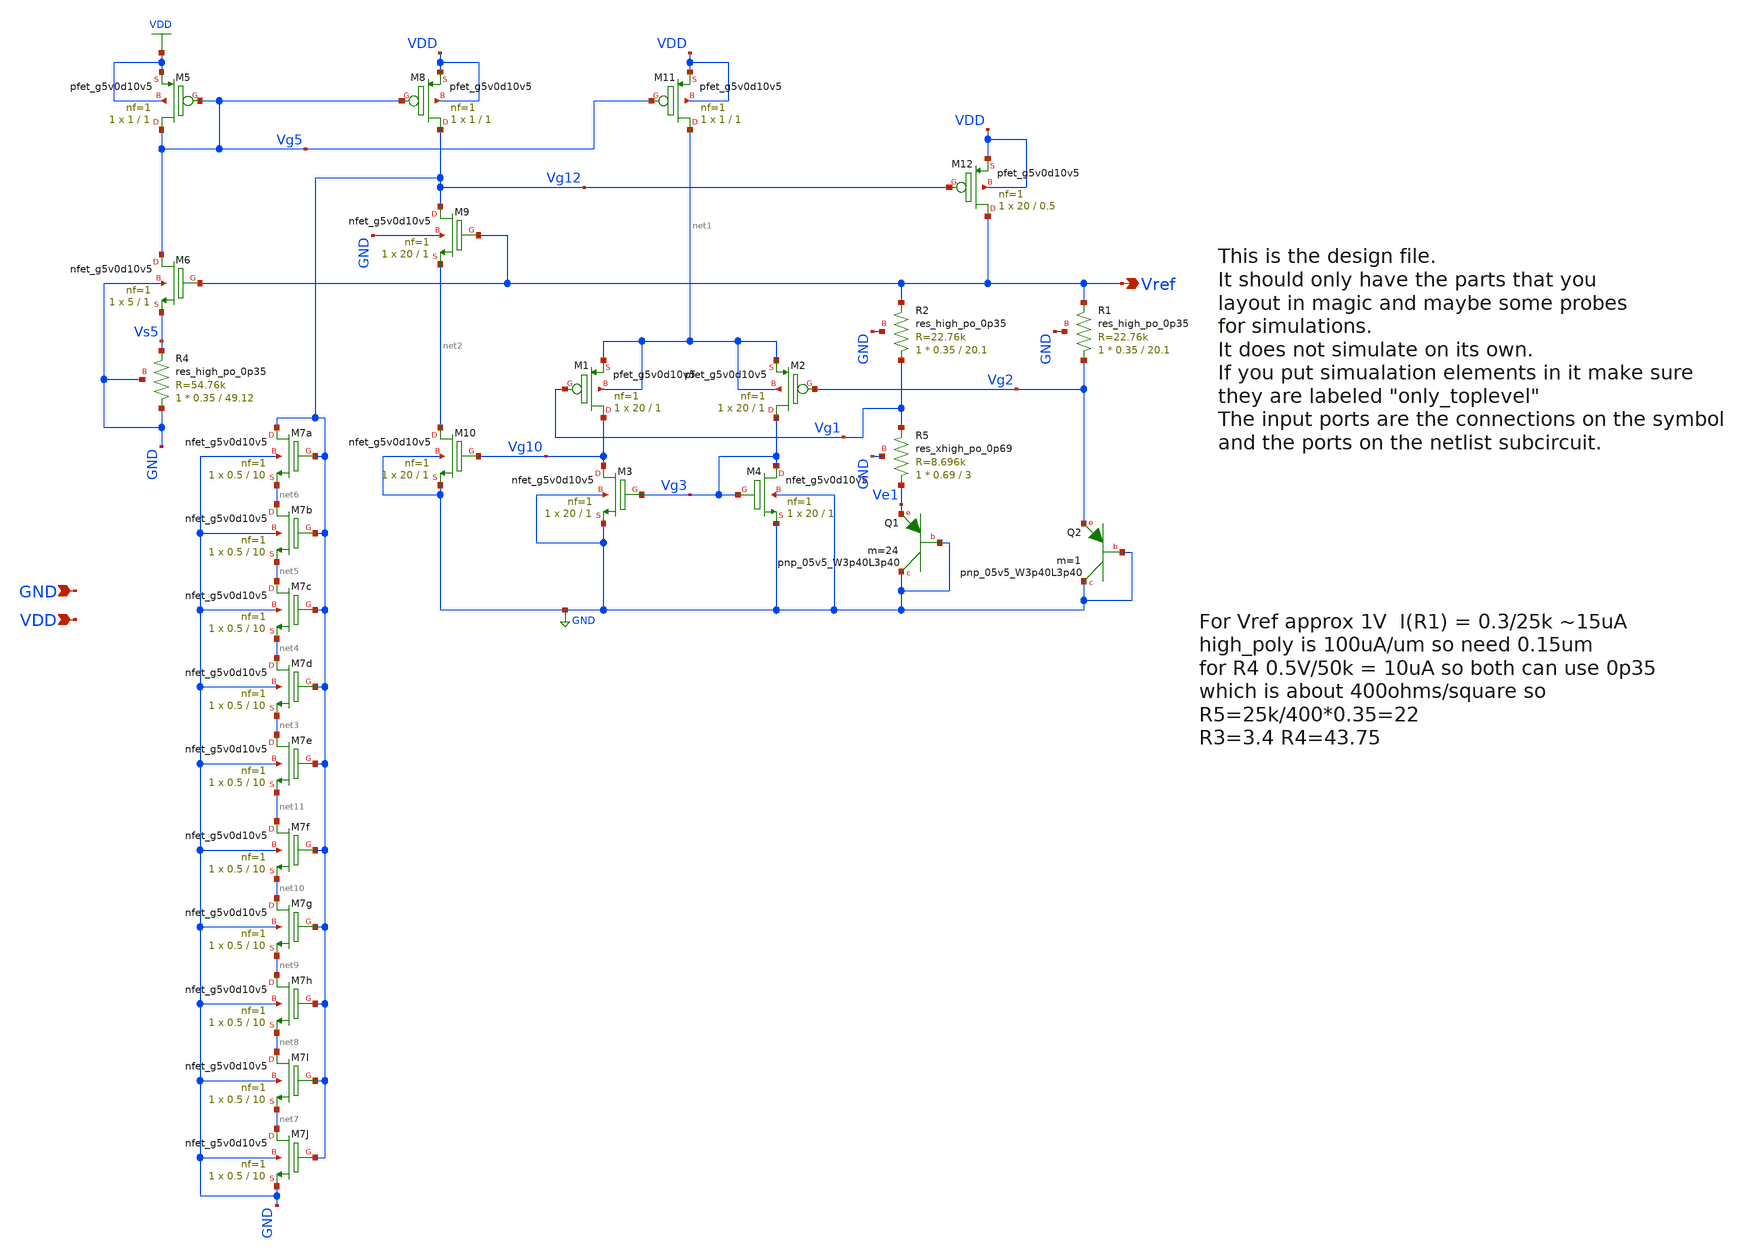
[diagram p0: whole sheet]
** sch_path: xschem/bandgap_x.sch
* Copyright 2021 Stefan Frederik Schippers
* Licensed under the Apache License, Version 2.0 (the "License");
* you may not use this file except in compliance with the License.
* You may obtain a copy of the License at
* https://www.apache.org/licenses/LICENSE-2.0
* Unless required by applicable law or agreed to in writing, software
* distributed under the License is distributed on an "AS IS" BASIS,
* WITHOUT WARRANTIES OR CONDITIONS OF ANY KIND, either express or implied.
* See the License for the specific language governing permissions and
* limitations under the License.
**.subckt bandgap_x Vref GND VDD
*.opin Vref
*.ipin GND
*.ipin VDD
XM4 Vg3 Vg3 GND GND sky130_fd_pr__nfet_g5v0d10v5 L=1 W=20 nf=1 ad='int((1 + 1)/2) * 20 / 1 * 0.29' as='int((1 + 2)/2) * 20 / 1 * 0.29'
+ pd='2*int((1 + 1)/2) * (20 / 1 + 0.29)' ps='2*int((1 + 2)/2) * (20 / 1 + 0.29)' nrd='0.29 / 20 ' nrs='0.29 / 20 '
+ sa=0 sb=0 sd=0 mult=1 m=1
XQ1 GND GND Ve1 sky130_fd_pr__pnp_05v5_W3p40L3p40 m=24
XQ2 GND GND Vg2 sky130_fd_pr__pnp_05v5_W3p40L3p40 m=1
XM1 Vg10 Vg1 net1 net1 sky130_fd_pr__pfet_g5v0d10v5 L=1 W=20 nf=1 ad='int((1 + 1)/2) * 20 / 1 * 0.29'
+ as='int((1 + 2)/2) * 20 / 1 * 0.29' pd='2*int((1 + 1)/2) * (20 / 1 + 0.29)' ps='2*int((1 + 2)/2) * (20 / 1 + 0.29)'
+ nrd='0.29 / 20 ' nrs='0.29 / 20 ' sa=0 sb=0 sd=0 mult=1 m=1
XM2 Vg3 Vg2 net1 net1 sky130_fd_pr__pfet_g5v0d10v5 L=1 W=20 nf=1 ad='int((1 + 1)/2) * 20 / 1 * 0.29'
+ as='int((1 + 2)/2) * 20 / 1 * 0.29' pd='2*int((1 + 1)/2) * (20 / 1 + 0.29)' ps='2*int((1 + 2)/2) * (20 / 1 + 0.29)'
+ nrd='0.29 / 20 ' nrs='0.29 / 20 ' sa=0 sb=0 sd=0 mult=1 m=1
XM11 net1 Vg5 VDD VDD sky130_fd_pr__pfet_g5v0d10v5 L=1 W=1 nf=1 ad='int((1 + 1)/2) * 1 / 1 * 0.29' as='int((1 + 2)/2) * 1 / 1 * 0.29'
+ pd='2*int((1 + 1)/2) * (1 / 1 + 0.29)' ps='2*int((1 + 2)/2) * (1 / 1 + 0.29)' nrd='0.29 / 1 ' nrs='0.29 / 1 '
+ sa=0 sb=0 sd=0 mult=1 m=1
XM3 Vg10 Vg3 GND GND sky130_fd_pr__nfet_g5v0d10v5 L=1 W=20 nf=1 ad='int((1 + 1)/2) * 20 / 1 * 0.29' as='int((1 + 2)/2) * 20 / 1 * 0.29'
+ pd='2*int((1 + 1)/2) * (20 / 1 + 0.29)' ps='2*int((1 + 2)/2) * (20 / 1 + 0.29)' nrd='0.29 / 20 ' nrs='0.29 / 20 '
+ sa=0 sb=0 sd=0 mult=1 m=1
XM10 net2 Vg10 GND GND sky130_fd_pr__nfet_g5v0d10v5 L=1 W=20 nf=1 ad='int((1 + 1)/2) * 20 / 1 * 0.29'
+ as='int((1 + 2)/2) * 20 / 1 * 0.29' pd='2*int((1 + 1)/2) * (20 / 1 + 0.29)' ps='2*int((1 + 2)/2) * (20 / 1 + 0.29)'
+ nrd='0.29 / 20 ' nrs='0.29 / 20 ' sa=0 sb=0 sd=0 mult=1 m=1
XM8 Vg12 Vg5 VDD VDD sky130_fd_pr__pfet_g5v0d10v5 L=1 W=1 nf=1 ad='int((1 + 1)/2) * 1 / 1 * 0.29' as='int((1 + 2)/2) * 1 / 1 * 0.29'
+ pd='2*int((1 + 1)/2) * (1 / 1 + 0.29)' ps='2*int((1 + 2)/2) * (1 / 1 + 0.29)' nrd='0.29 / 1 ' nrs='0.29 / 1 '
+ sa=0 sb=0 sd=0 mult=1 m=1
XM5 Vg5 Vg5 VDD VDD sky130_fd_pr__pfet_g5v0d10v5 L=1 W=1 nf=1 ad='int((1 + 1)/2) * 1 / 1 * 0.29' as='int((1 + 2)/2) * 1 / 1 * 0.29'
+ pd='2*int((1 + 1)/2) * (1 / 1 + 0.29)' ps='2*int((1 + 2)/2) * (1 / 1 + 0.29)' nrd='0.29 / 1 ' nrs='0.29 / 1 '
+ sa=0 sb=0 sd=0 mult=1 m=1
XM12 Vref Vg12 VDD VDD sky130_fd_pr__pfet_g5v0d10v5 L=0.5 W=20 nf=1 ad='int((1 + 1)/2) * 20 / 1 * 0.29'
+ as='int((1 + 2)/2) * 20 / 1 * 0.29' pd='2*int((1 + 1)/2) * (20 / 1 + 0.29)' ps='2*int((1 + 2)/2) * (20 / 1 + 0.29)'
+ nrd='0.29 / 20 ' nrs='0.29 / 20 ' sa=0 sb=0 sd=0 mult=1 m=1
XM9 Vg12 Vref net2 GND sky130_fd_pr__nfet_g5v0d10v5 L=1 W=20 nf=1 ad='int((1 + 1)/2) * 20 / 1 * 0.29'
+ as='int((1 + 2)/2) * 20 / 1 * 0.29' pd='2*int((1 + 1)/2) * (20 / 1 + 0.29)' ps='2*int((1 + 2)/2) * (20 / 1 + 0.29)'
+ nrd='0.29 / 20 ' nrs='0.29 / 20 ' sa=0 sb=0 sd=0 mult=1 m=1
XM7a Vg12 Vg12 net6 GND sky130_fd_pr__nfet_g5v0d10v5 L=10 W=0.5 nf=1 ad='int((1 + 1)/2) * 0.5 / 1 * 0.29'
+ as='int((1 + 2)/2) * 0.5 / 1 * 0.29' pd='2*int((1 + 1)/2) * (0.5 / 1 + 0.29)' ps='2*int((1 + 2)/2) * (0.5 / 1 + 0.29)'
+ nrd='0.29 / 0.5 ' nrs='0.29 / 0.5 ' sa=0 sb=0 sd=0 mult=1 m=1
XM7b net6 Vg12 net5 GND sky130_fd_pr__nfet_g5v0d10v5 L=10 W=0.5 nf=1 ad='int((1 + 1)/2) * 0.5 / 1 * 0.29'
+ as='int((1 + 2)/2) * 0.5 / 1 * 0.29' pd='2*int((1 + 1)/2) * (0.5 / 1 + 0.29)' ps='2*int((1 + 2)/2) * (0.5 / 1 + 0.29)'
+ nrd='0.29 / 0.5 ' nrs='0.29 / 0.5 ' sa=0 sb=0 sd=0 mult=1 m=1
XM7c net5 Vg12 net4 GND sky130_fd_pr__nfet_g5v0d10v5 L=10 W=0.5 nf=1 ad='int((1 + 1)/2) * 0.5 / 1 * 0.29'
+ as='int((1 + 2)/2) * 0.5 / 1 * 0.29' pd='2*int((1 + 1)/2) * (0.5 / 1 + 0.29)' ps='2*int((1 + 2)/2) * (0.5 / 1 + 0.29)'
+ nrd='0.29 / 0.5 ' nrs='0.29 / 0.5 ' sa=0 sb=0 sd=0 mult=1 m=1
XM7d net4 Vg12 net3 GND sky130_fd_pr__nfet_g5v0d10v5 L=10 W=0.5 nf=1 ad='int((1 + 1)/2) * 0.5 / 1 * 0.29'
+ as='int((1 + 2)/2) * 0.5 / 1 * 0.29' pd='2*int((1 + 1)/2) * (0.5 / 1 + 0.29)' ps='2*int((1 + 2)/2) * (0.5 / 1 + 0.29)'
+ nrd='0.29 / 0.5 ' nrs='0.29 / 0.5 ' sa=0 sb=0 sd=0 mult=1 m=1
XM7e net3 Vg12 net11 GND sky130_fd_pr__nfet_g5v0d10v5 L=10 W=0.5 nf=1 ad='int((1 + 1)/2) * 0.5 / 1 * 0.29'
+ as='int((1 + 2)/2) * 0.5 / 1 * 0.29' pd='2*int((1 + 1)/2) * (0.5 / 1 + 0.29)' ps='2*int((1 + 2)/2) * (0.5 / 1 + 0.29)'
+ nrd='0.29 / 0.5 ' nrs='0.29 / 0.5 ' sa=0 sb=0 sd=0 mult=1 m=1
XM6 Vg5 Vref Vs5 GND sky130_fd_pr__nfet_g5v0d10v5 L=1 W=5 nf=1 ad='int((1 + 1)/2) * 5 / 1 * 0.29' as='int((1 + 2)/2) * 5 / 1 * 0.29'
+ pd='2*int((1 + 1)/2) * (5 / 1 + 0.29)' ps='2*int((1 + 2)/2) * (5 / 1 + 0.29)' nrd='0.29 / 5 ' nrs='0.29 / 5 '
+ sa=0 sb=0 sd=0 mult=1 m=1
XR1 Vg2 Vref GND sky130_fd_pr__res_high_po_0p35 L=20.1 mult=1 m=1
XR2 Vg1 Vref GND sky130_fd_pr__res_high_po_0p35 L=20.1 mult=1 m=1
XR4 GND Vs5 GND sky130_fd_pr__res_high_po_0p35 L=49.12 mult=1 m=1
XM7f net11 Vg12 net10 GND sky130_fd_pr__nfet_g5v0d10v5 L=10 W=0.5 nf=1 ad='int((1 + 1)/2) * 0.5 / 1 * 0.29'
+ as='int((1 + 2)/2) * 0.5 / 1 * 0.29' pd='2*int((1 + 1)/2) * (0.5 / 1 + 0.29)' ps='2*int((1 + 2)/2) * (0.5 / 1 + 0.29)'
+ nrd='0.29 / 0.5 ' nrs='0.29 / 0.5 ' sa=0 sb=0 sd=0 mult=1 m=1
XM7g net10 Vg12 net9 GND sky130_fd_pr__nfet_g5v0d10v5 L=10 W=0.5 nf=1 ad='int((1 + 1)/2) * 0.5 / 1 * 0.29'
+ as='int((1 + 2)/2) * 0.5 / 1 * 0.29' pd='2*int((1 + 1)/2) * (0.5 / 1 + 0.29)' ps='2*int((1 + 2)/2) * (0.5 / 1 + 0.29)'
+ nrd='0.29 / 0.5 ' nrs='0.29 / 0.5 ' sa=0 sb=0 sd=0 mult=1 m=1
XM7h net9 Vg12 net8 GND sky130_fd_pr__nfet_g5v0d10v5 L=10 W=0.5 nf=1 ad='int((1 + 1)/2) * 0.5 / 1 * 0.29'
+ as='int((1 + 2)/2) * 0.5 / 1 * 0.29' pd='2*int((1 + 1)/2) * (0.5 / 1 + 0.29)' ps='2*int((1 + 2)/2) * (0.5 / 1 + 0.29)'
+ nrd='0.29 / 0.5 ' nrs='0.29 / 0.5 ' sa=0 sb=0 sd=0 mult=1 m=1
XM7I net8 Vg12 net7 GND sky130_fd_pr__nfet_g5v0d10v5 L=10 W=0.5 nf=1 ad='int((1 + 1)/2) * 0.5 / 1 * 0.29'
+ as='int((1 + 2)/2) * 0.5 / 1 * 0.29' pd='2*int((1 + 1)/2) * (0.5 / 1 + 0.29)' ps='2*int((1 + 2)/2) * (0.5 / 1 + 0.29)'
+ nrd='0.29 / 0.5 ' nrs='0.29 / 0.5 ' sa=0 sb=0 sd=0 mult=1 m=1
XM7J net7 Vg12 GND GND sky130_fd_pr__nfet_g5v0d10v5 L=10 W=0.5 nf=1 ad='int((1 + 1)/2) * 0.5 / 1 * 0.29'
+ as='int((1 + 2)/2) * 0.5 / 1 * 0.29' pd='2*int((1 + 1)/2) * (0.5 / 1 + 0.29)' ps='2*int((1 + 2)/2) * (0.5 / 1 + 0.29)'
+ nrd='0.29 / 0.5 ' nrs='0.29 / 0.5 ' sa=0 sb=0 sd=0 mult=1 m=1
XR5 Ve1 Vg1 GND sky130_fd_pr__res_xhigh_po_0p69 L=3 mult=1 m=1
**.ends
.GLOBAL GND
.GLOBAL VDD
.end
